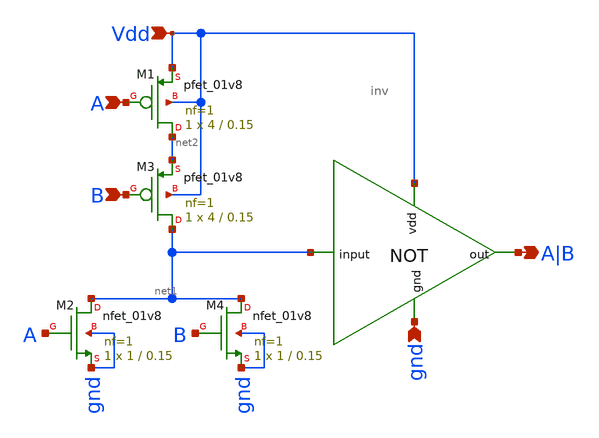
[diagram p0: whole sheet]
** sch_path: schematics/or.sch
**.subckt or A B Vdd gnd A|B
*.ipin A
*.ipin B
*.ipin Vdd
*.ipin gnd
*.opin A|B
XM1 net2 A Vdd Vdd sky130_fd_pr__pfet_01v8 L=0.15 W=4 nf=1 ad='int((1 + 1)/2) * 4 / 1 * 0.29' as='int((1 + 2)/2) * 4 / 1 * 0.29'
+ pd='2*int((1 + 1)/2) * (4 / 1 + 0.29)' ps='2*int((1 + 2)/2) * (4 / 1 + 0.29)' nrd='0.29 / 4 ' nrs='0.29 / 4 '
+ sa=0 sb=0 sd=0 mult=1 m=1
XM2 net1 A gnd gnd sky130_fd_pr__nfet_01v8 L=0.15 W=1 nf=1 ad='int((1 + 1)/2) * 1 / 1 * 0.29' as='int((1 + 2)/2) * 1 / 1 * 0.29'
+ pd='2*int((1 + 1)/2) * (1 / 1 + 0.29)' ps='2*int((1 + 2)/2) * (1 / 1 + 0.29)' nrd='0.29 / 1 ' nrs='0.29 / 1 '
+ sa=0 sb=0 sd=0 mult=1 m=1
XM3 net1 B net2 Vdd sky130_fd_pr__pfet_01v8 L=0.15 W=4 nf=1 ad='int((1 + 1)/2) * 4 / 1 * 0.29' as='int((1 + 2)/2) * 4 / 1 * 0.29'
+ pd='2*int((1 + 1)/2) * (4 / 1 + 0.29)' ps='2*int((1 + 2)/2) * (4 / 1 + 0.29)' nrd='0.29 / 4 ' nrs='0.29 / 4 '
+ sa=0 sb=0 sd=0 mult=1 m=1
XM4 net1 B gnd gnd sky130_fd_pr__nfet_01v8 L=0.15 W=1 nf=1 ad='int((1 + 1)/2) * 1 / 1 * 0.29' as='int((1 + 2)/2) * 1 / 1 * 0.29'
+ pd='2*int((1 + 1)/2) * (1 / 1 + 0.29)' ps='2*int((1 + 2)/2) * (1 / 1 + 0.29)' nrd='0.29 / 1 ' nrs='0.29 / 1 '
+ sa=0 sb=0 sd=0 mult=1 m=1
x1 A|B Vdd net1 gnd inv
**.ends
.end
